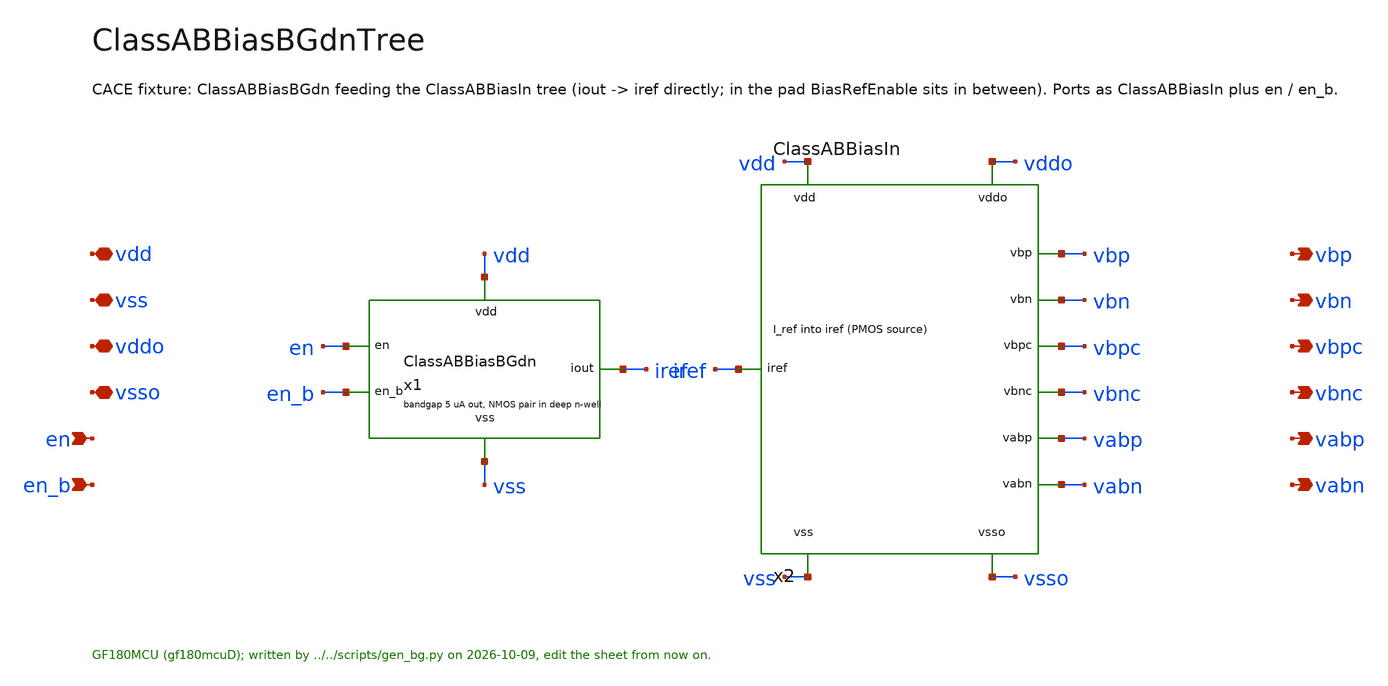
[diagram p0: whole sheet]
** sch_path: macros/ClassABBias/schematic/xschem/ClassABBiasBGdnTree.sch
**.subckt ClassABBiasBGdnTree vdd vss vddo vsso en en_b vbp vbn vbpc vbnc vabp vabn
*.iopin vdd
*.iopin vss
*.iopin vddo
*.iopin vsso
*.ipin en
*.ipin en_b
*.opin vbp
*.opin vbn
*.opin vbpc
*.opin vbnc
*.opin vabp
*.opin vabn
x1 vdd vss iref en en_b ClassABBiasBGdn
x2 vdd vss vddo vsso iref vbp vbn vbpc vbnc vabp vabn ClassABBiasIn
**.ends

* expanding   symbol:  ClassABBiasBGdn.sym # of pins=5
** sym_path: macros/ClassABBias/schematic/xschem/ClassABBiasBGdn.sym
** sch_path: macros/ClassABBias/schematic/xschem/ClassABBiasBGdn.sch
.subckt ClassABBiasBGdn vdd vss iout en en_b
*.iopin vdd
*.iopin vss
*.ipin en
*.ipin en_b
*.iopin iout
XE vdd vss en en_b vpg ks RefCoreEnable
XMS1 ks en_b vdd vdd pfet_03v3 L=50u W=0.22u nf=1 ad='int((nf+1)/2) * W/nf * 0.18u' as='int((nf+2)/2) * W/nf * 0.18u'
+ pd='2*int((nf+1)/2) * (W/nf + 0.18u)' ps='2*int((nf+2)/2) * (W/nf + 0.18u)' nrd='0.18u / W' nrs='0.18u / W'
+ sa=0 sb=0 sd=0 m=1
XMS3 vpg ks vss vss nfet_03v3 L=2u W=0.5u nf=1 ad='int((nf+1)/2) * W/nf * 0.18u' as='int((nf+2)/2) * W/nf * 0.18u'
+ pd='2*int((nf+1)/2) * (W/nf + 0.18u)' ps='2*int((nf+2)/2) * (W/nf + 0.18u)' nrd='0.18u / W' nrs='0.18u / W'
+ sa=0 sb=0 sd=0 m=1
XMS2 ks g vss vss nfet_03v3 L=1u W=10u nf=1 ad='int((nf+1)/2) * W/nf * 0.18u' as='int((nf+2)/2) * W/nf * 0.18u'
+ pd='2*int((nf+1)/2) * (W/nf + 0.18u)' ps='2*int((nf+2)/2) * (W/nf + 0.18u)' nrd='0.18u / W' nrs='0.18u / W'
+ sa=0 sb=0 sd=0 m=1
XPB cb vpg vdd vdd pfet_03v3 L=4u W=48u nf=4 ad='int((nf+1)/2) * W/nf * 0.18u' as='int((nf+2)/2) * W/nf * 0.18u'
+ pd='2*int((nf+1)/2) * (W/nf + 0.18u)' ps='2*int((nf+2)/2) * (W/nf + 0.18u)' nrd='0.18u / W' nrs='0.18u / W'
+ sa=0 sb=0 sd=0 m=1
XPBC vpg vpc cb vdd pfet_03v3 L=2u W=48u nf=4 ad='int((nf+1)/2) * W/nf * 0.18u' as='int((nf+2)/2) * W/nf * 0.18u'
+ pd='2*int((nf+1)/2) * (W/nf + 0.18u)' ps='2*int((nf+2)/2) * (W/nf + 0.18u)' nrd='0.18u / W' nrs='0.18u / W'
+ sa=0 sb=0 sd=0 m=1
XNB vpc g eb eb nfet_03v3 L=12u W=20u nf=2 ad='int((nf+1)/2) * W/nf * 0.18u' as='int((nf+2)/2) * W/nf * 0.18u'
+ pd='2*int((nf+1)/2) * (W/nf + 0.18u)' ps='2*int((nf+2)/2) * (W/nf + 0.18u)' nrd='0.18u / W' nrs='0.18u / W'
+ sa=0 sb=0 sd=0 m=1
XR1B vss eb vss ppolyf_u_3k r_width=1u r_length=107.4u m=1
XR0 e2 eb vss ppolyf_u_3k r_width=1u r_length=32.8u m=1
XQ2 vss vss e2 pnp_05p00x05p00 m=8 par=8
XRC vpc vpg vss ppolyf_u_3k r_width=1u r_length=50u m=1
XPA ca vpg vdd vdd pfet_03v3 L=4u W=48u nf=4 ad='int((nf+1)/2) * W/nf * 0.18u' as='int((nf+2)/2) * W/nf * 0.18u'
+ pd='2*int((nf+1)/2) * (W/nf + 0.18u)' ps='2*int((nf+2)/2) * (W/nf + 0.18u)' nrd='0.18u / W' nrs='0.18u / W'
+ sa=0 sb=0 sd=0 m=1
XPAC g vpc ca vdd pfet_03v3 L=2u W=48u nf=4 ad='int((nf+1)/2) * W/nf * 0.18u' as='int((nf+2)/2) * W/nf * 0.18u'
+ pd='2*int((nf+1)/2) * (W/nf + 0.18u)' ps='2*int((nf+2)/2) * (W/nf + 0.18u)' nrd='0.18u / W' nrs='0.18u / W'
+ sa=0 sb=0 sd=0 m=1
XNA g g ea ea nfet_03v3 L=12u W=20u nf=2 ad='int((nf+1)/2) * W/nf * 0.18u' as='int((nf+2)/2) * W/nf * 0.18u'
+ pd='2*int((nf+1)/2) * (W/nf + 0.18u)' ps='2*int((nf+2)/2) * (W/nf + 0.18u)' nrd='0.18u / W' nrs='0.18u / W'
+ sa=0 sb=0 sd=0 m=1
XR1A vss ea vss ppolyf_u_3k r_width=1u r_length=118.1u m=1
XQ1 vss vss ea pnp_05p00x05p00 m=1 par=1
XPO co vpg vdd vdd pfet_03v3 L=4u W=96u nf=8 ad='int((nf+1)/2) * W/nf * 0.18u' as='int((nf+2)/2) * W/nf * 0.18u'
+ pd='2*int((nf+1)/2) * (W/nf + 0.18u)' ps='2*int((nf+2)/2) * (W/nf + 0.18u)' nrd='0.18u / W' nrs='0.18u / W'
+ sa=0 sb=0 sd=0 m=1
XPOC iout vpc co vdd pfet_03v3 L=2u W=96u nf=8 ad='int((nf+1)/2) * W/nf * 0.18u' as='int((nf+2)/2) * W/nf * 0.18u'
+ pd='2*int((nf+1)/2) * (W/nf + 0.18u)' ps='2*int((nf+2)/2) * (W/nf + 0.18u)' nrd='0.18u / W' nrs='0.18u / W'
+ sa=0 sb=0 sd=0 m=1
DPWA ea vdd diode_pw2dw area='12u * 30u ' pj='2*12u + 2*30u ' m=1
DPWB eb vdd diode_pw2dw area='12u * 30u ' pj='2*12u + 2*30u ' m=1
DDNW vss vdd diode_dw2ps area='30u * 60u ' pj='2*30u + 2*60u ' m=1
.ends


* expanding   symbol:  ClassABBiasIn.sym # of pins=11
** sym_path: macros/ClassABBias/schematic/xschem/ClassABBiasIn.sym
** sch_path: macros/ClassABBias/schematic/xschem/ClassABBiasIn.sch
.subckt ClassABBiasIn vdd vss vddo vsso iref vbp vbn vbpc vbnc vabp vabn
*.iopin vdd
*.iopin vss
*.iopin vddo
*.iopin vsso
*.iopin iref
*.opin vbp
*.opin vbn
*.opin vbpc
*.opin vbnc
*.opin vabp
*.opin vabn
XNI iref iref vss vss nfet_03v3 L=6u W=6u nf=1 ad='int((nf+1)/2) * W/nf * 0.18u' as='int((nf+2)/2) * W/nf * 0.18u'
+ pd='2*int((nf+1)/2) * (W/nf + 0.18u)' ps='2*int((nf+2)/2) * (W/nf + 0.18u)' nrd='0.18u / W' nrs='0.18u / W'
+ sa=0 sb=0 sd=0 m=1
XBPC vbpc vbpc vdd vdd pfet_03v3 L=4u W=1u nf=1 ad='int((nf+1)/2) * W/nf * 0.18u' as='int((nf+2)/2) * W/nf * 0.18u'
+ pd='2*int((nf+1)/2) * (W/nf + 0.18u)' ps='2*int((nf+2)/2) * (W/nf + 0.18u)' nrd='0.18u / W' nrs='0.18u / W'
+ sa=0 sb=0 sd=0 m=1
XNBPC vbpc iref vss vss nfet_03v3 L=6u W=2.5u nf=1 ad='int((nf+1)/2) * W/nf * 0.18u' as='int((nf+2)/2) * W/nf * 0.18u'
+ pd='2*int((nf+1)/2) * (W/nf + 0.18u)' ps='2*int((nf+2)/2) * (W/nf + 0.18u)' nrd='0.18u / W' nrs='0.18u / W'
+ sa=0 sb=0 sd=0 m=1
XBP vbp vbp vdd vdd pfet_03v3 L=6u W=20u nf=2 ad='int((nf+1)/2) * W/nf * 0.18u' as='int((nf+2)/2) * W/nf * 0.18u'
+ pd='2*int((nf+1)/2) * (W/nf + 0.18u)' ps='2*int((nf+2)/2) * (W/nf + 0.18u)' nrd='0.18u / W' nrs='0.18u / W'
+ sa=0 sb=0 sd=0 m=1
XNBP vbp iref vss vss nfet_03v3 L=6u W=6u nf=1 ad='int((nf+1)/2) * W/nf * 0.18u' as='int((nf+2)/2) * W/nf * 0.18u'
+ pd='2*int((nf+1)/2) * (W/nf + 0.18u)' ps='2*int((nf+2)/2) * (W/nf + 0.18u)' nrd='0.18u / W' nrs='0.18u / W'
+ sa=0 sb=0 sd=0 m=1
XRP1 n1 n1 vddo vddo pfet_03v3 L=0.6u W=12u nf=2 ad='int((nf+1)/2) * W/nf * 0.18u' as='int((nf+2)/2) * W/nf * 0.18u'
+ pd='2*int((nf+1)/2) * (W/nf + 0.18u)' ps='2*int((nf+2)/2) * (W/nf + 0.18u)' nrd='0.18u / W' nrs='0.18u / W'
+ sa=0 sb=0 sd=0 m=1
XRP2 vabp vabp n1 vdd pfet_03v3 L=0.6u W=6.66u nf=1 ad='int((nf+1)/2) * W/nf * 0.18u' as='int((nf+2)/2) * W/nf * 0.18u'
+ pd='2*int((nf+1)/2) * (W/nf + 0.18u)' ps='2*int((nf+2)/2) * (W/nf + 0.18u)' nrd='0.18u / W' nrs='0.18u / W'
+ sa=0 sb=0 sd=0 m=1
XNABP vabp iref vss vss nfet_03v3 L=6u W=6u nf=1 ad='int((nf+1)/2) * W/nf * 0.18u' as='int((nf+2)/2) * W/nf * 0.18u'
+ pd='2*int((nf+1)/2) * (W/nf + 0.18u)' ps='2*int((nf+2)/2) * (W/nf + 0.18u)' nrd='0.18u / W' nrs='0.18u / W'
+ sa=0 sb=0 sd=0 m=1
XPBNC vbnc vbp vdd vdd pfet_03v3 L=6u W=8u nf=1 ad='int((nf+1)/2) * W/nf * 0.18u' as='int((nf+2)/2) * W/nf * 0.18u'
+ pd='2*int((nf+1)/2) * (W/nf + 0.18u)' ps='2*int((nf+2)/2) * (W/nf + 0.18u)' nrd='0.18u / W' nrs='0.18u / W'
+ sa=0 sb=0 sd=0 m=1
XBNC vbnc vbnc vss vss nfet_03v3 L=8u W=1u nf=1 ad='int((nf+1)/2) * W/nf * 0.18u' as='int((nf+2)/2) * W/nf * 0.18u'
+ pd='2*int((nf+1)/2) * (W/nf + 0.18u)' ps='2*int((nf+2)/2) * (W/nf + 0.18u)' nrd='0.18u / W' nrs='0.18u / W'
+ sa=0 sb=0 sd=0 m=1
XPBN vbn vbp vdd vdd pfet_03v3 L=6u W=20u nf=2 ad='int((nf+1)/2) * W/nf * 0.18u' as='int((nf+2)/2) * W/nf * 0.18u'
+ pd='2*int((nf+1)/2) * (W/nf + 0.18u)' ps='2*int((nf+2)/2) * (W/nf + 0.18u)' nrd='0.18u / W' nrs='0.18u / W'
+ sa=0 sb=0 sd=0 m=1
XBN vbn vbn vss vss nfet_03v3 L=6u W=6u nf=1 ad='int((nf+1)/2) * W/nf * 0.18u' as='int((nf+2)/2) * W/nf * 0.18u'
+ pd='2*int((nf+1)/2) * (W/nf + 0.18u)' ps='2*int((nf+2)/2) * (W/nf + 0.18u)' nrd='0.18u / W' nrs='0.18u / W'
+ sa=0 sb=0 sd=0 m=1
XPABN vabn vbp vdd vdd pfet_03v3 L=6u W=20u nf=2 ad='int((nf+1)/2) * W/nf * 0.18u' as='int((nf+2)/2) * W/nf * 0.18u'
+ pd='2*int((nf+1)/2) * (W/nf + 0.18u)' ps='2*int((nf+2)/2) * (W/nf + 0.18u)' nrd='0.18u / W' nrs='0.18u / W'
+ sa=0 sb=0 sd=0 m=1
XRN2 vabn vabn n2 vss nfet_03v3 L=1u W=4.4u nf=1 ad='int((nf+1)/2) * W/nf * 0.18u' as='int((nf+2)/2) * W/nf * 0.18u'
+ pd='2*int((nf+1)/2) * (W/nf + 0.18u)' ps='2*int((nf+2)/2) * (W/nf + 0.18u)' nrd='0.18u / W' nrs='0.18u / W'
+ sa=0 sb=0 sd=0 m=1
XRN1 n2 n2 vsso vsso nfet_03v3 L=1u W=8u nf=2 ad='int((nf+1)/2) * W/nf * 0.18u' as='int((nf+2)/2) * W/nf * 0.18u'
+ pd='2*int((nf+1)/2) * (W/nf + 0.18u)' ps='2*int((nf+2)/2) * (W/nf + 0.18u)' nrd='0.18u / W' nrs='0.18u / W'
+ sa=0 sb=0 sd=0 m=1
.ends


* expanding   symbol:  RefCoreEnable.sym # of pins=6
** sym_path: macros/PadEnable/schematic/xschem/RefCoreEnable.sym
** sch_path: macros/PadEnable/schematic/xschem/RefCoreEnable.sch
.subckt RefCoreEnable vdd vss en en_b vpg ks
*.iopin vdd
*.iopin vss
*.ipin en
*.ipin en_b
*.iopin vpg
*.iopin ks
XSPG vpg en vdd vdd pfet_03v3 L=0.5u W=1u nf=1 ad='int((nf+1)/2) * W/nf * 0.18u' as='int((nf+2)/2) * W/nf * 0.18u'
+ pd='2*int((nf+1)/2) * (W/nf + 0.18u)' ps='2*int((nf+2)/2) * (W/nf + 0.18u)' nrd='0.18u / W' nrs='0.18u / W'
+ sa=0 sb=0 sd=0 m=1
XSKS ks en_b vss vss nfet_03v3 L=0.5u W=1u nf=1 ad='int((nf+1)/2) * W/nf * 0.18u' as='int((nf+2)/2) * W/nf * 0.18u'
+ pd='2*int((nf+1)/2) * (W/nf + 0.18u)' ps='2*int((nf+2)/2) * (W/nf + 0.18u)' nrd='0.18u / W' nrs='0.18u / W'
+ sa=0 sb=0 sd=0 m=1
.ends

.end
